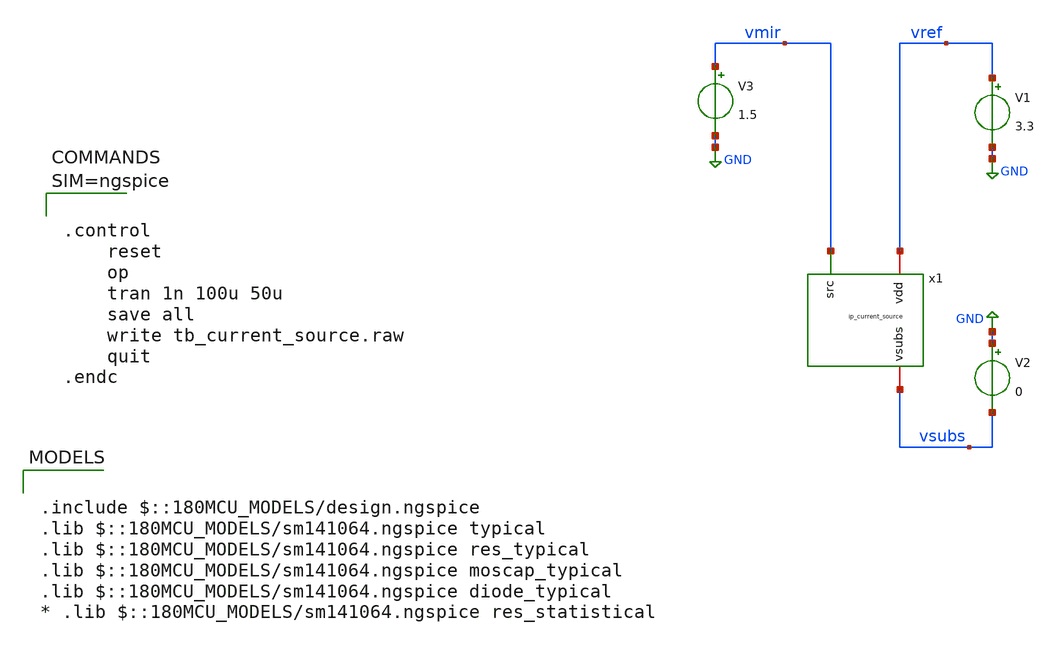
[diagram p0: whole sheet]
** sch_path: xschem/tb_current_source.sch
**.subckt tb_current_source
x1 vref vmir vsubs ip_current_source
V1 vref GND 3.3
V2 GND vsubs 0
V3 vmir GND 1.5
**** begin user architecture code

.include $::180MCU_MODELS/design.ngspice
.lib $::180MCU_MODELS/sm141064.ngspice typical
.lib $::180MCU_MODELS/sm141064.ngspice res_typical
.lib $::180MCU_MODELS/sm141064.ngspice moscap_typical
.lib $::180MCU_MODELS/sm141064.ngspice diode_typical
* .lib $::180MCU_MODELS/sm141064.ngspice res_statistical




.control
	reset
	op
	tran 1n 100u 50u
	save all
	write tb_current_source.raw
	quit
.endc



**** end user architecture code
**.ends

* expanding   symbol:  ip_current_source.sym # of pins=3
** sym_path: xschem/ip_current_source.sym
** sch_path: xschem/ip_current_source.sch
.subckt ip_current_source vdd src vsubs
*.iopin vdd
*.iopin vsubs
*.ipin src
XM1 net1 net1 vsubs vsubs nfet_03v3 L=1u W=3u nf=1 ad='int((nf+1)/2) * W/nf * 0.18u' as='int((nf+2)/2) * W/nf * 0.18u'
+ pd='2*int((nf+1)/2) * (W/nf + 0.18u)' ps='2*int((nf+2)/2) * (W/nf + 0.18u)' nrd='0.18u / W' nrs='0.18u / W'
+ sa=0 sb=0 sd=0 m=1
XM2 net2 net1 vsubs vsubs nfet_03v3 L=10u W=0.3u nf=1 ad='int((nf+1)/2) * W/nf * 0.18u' as='int((nf+2)/2) * W/nf * 0.18u'
+ pd='2*int((nf+1)/2) * (W/nf + 0.18u)' ps='2*int((nf+2)/2) * (W/nf + 0.18u)' nrd='0.18u / W' nrs='0.18u / W'
+ sa=0 sb=0 sd=0 m=1
XR2 vdd net1 vsubs ppolyf_u_3k r_width=1e-6 r_length=6e-6 m=1
XM3 src net1 net2 vsubs nfet_03v3 L=0.3u W=10u nf=1 ad='int((nf+1)/2) * W/nf * 0.18u' as='int((nf+2)/2) * W/nf * 0.18u'
+ pd='2*int((nf+1)/2) * (W/nf + 0.18u)' ps='2*int((nf+2)/2) * (W/nf + 0.18u)' nrd='0.18u / W' nrs='0.18u / W'
+ sa=0 sb=0 sd=0 m=1
.ends

.GLOBAL GND
.end
